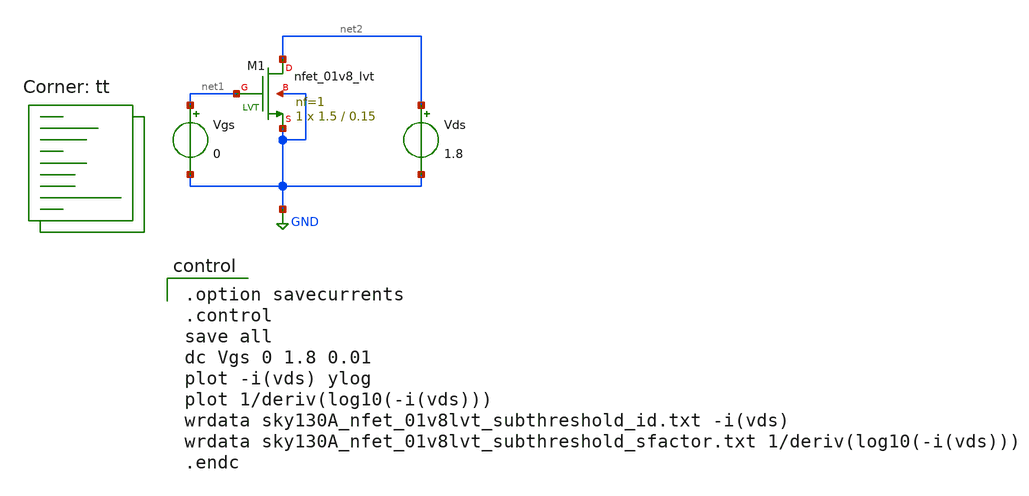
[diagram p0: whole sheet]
** sch_path: xschem/MOSFET/sky130A_nfet_01v8lvt_subthreshold.sch
**.subckt sky130A_nfet_01v8lvt_subthreshold
Vgs net1 GND 0
Vds net2 GND 1.8
XM1 net2 net1 GND GND sky130_fd_pr__nfet_01v8_lvt L=0.15 W=1.5 nf=1 ad='int((1 + 1)/2) * 1.5 / 1 * 0.29'
+ as='int((1 + 2)/2) * 1.5 / 1 * 0.29' pd='2*int((1 + 1)/2) * (1.5 / 1 + 0.29)' ps='2*int((1 + 2)/2) * (1.5 / 1 + 0.29)'
+ nrd='0.29 / 1.5 ' nrs='0.29 / 1.5 ' sa=0 sb=0 sd=0 mult=1 m=1
**** begin user architecture code

.option savecurrents
.control
save all
dc Vgs 0 1.8 0.01
plot -i(vds) ylog
plot 1/deriv(log10(-i(vds)))
wrdata sky130A_nfet_01v8lvt_subthreshold_id.txt -i(vds)
wrdata sky130A_nfet_01v8lvt_subthreshold_sfactor.txt 1/deriv(log10(-i(vds)))
.endc

.lib $::SKYWATER_MODELS/sky130.lib.spice tt
**** end user architecture code
**.ends
.GLOBAL GND
.end
